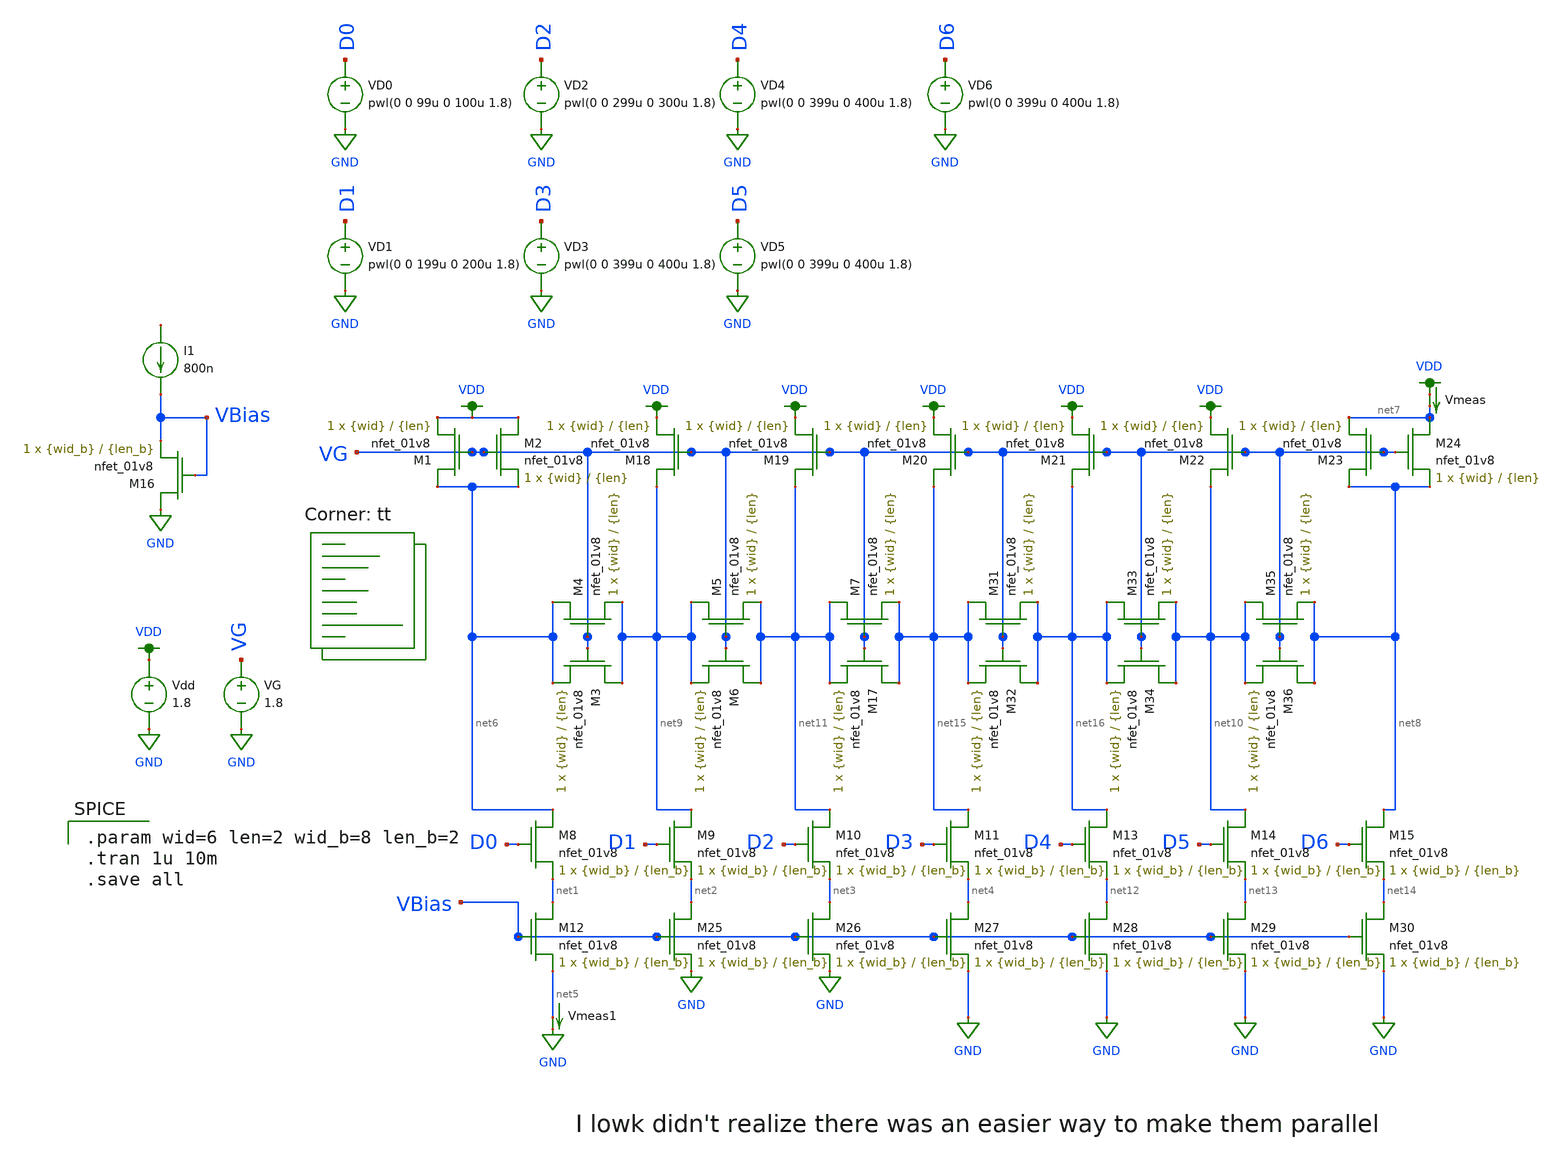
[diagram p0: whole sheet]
** sch_path: mp3/ladder_tb.sch
**.subckt ladder_tb
XM8 net6 D0 net1 GND sky130_fd_pr__nfet_01v8 L={len_b} W={wid_b} nf=1 ad='int((nf+1)/2) * W/nf * 0.29'
+ as='int((nf+2)/2) * W/nf * 0.29' pd='2*int((nf+1)/2) * (W/nf + 0.29)' ps='2*int((nf+2)/2) * (W/nf + 0.29)'
+ nrd='0.29 / W' nrs='0.29 / W' sa=0 sb=0 sd=0 mult=1 m=1
Vmeas1 net5 GND 0
.save i(vmeas1)
Vdd VDD GND 1.8
VG VG GND 1.8
VD0 D0 GND pwl(0 0 99u 0 100u 1.8)
VD1 D1 GND pwl(0 0 199u 0 200u 1.8)
VD2 D2 GND pwl(0 0 299u 0 300u 1.8)
VD3 D3 GND pwl(0 0 399u 0 400u 1.8)
XM16 GND VBias VBias GND sky130_fd_pr__nfet_01v8 L={len_b} W={wid_b} nf=1 ad='int((nf+1)/2) * W/nf * 0.29'
+ as='int((nf+2)/2) * W/nf * 0.29' pd='2*int((nf+1)/2) * (W/nf + 0.29)' ps='2*int((nf+2)/2) * (W/nf + 0.29)'
+ nrd='0.29 / W' nrs='0.29 / W' sa=0 sb=0 sd=0 mult=1 m=1
I1 net17 VBias 800n
XM1 net6 VG VDD GND sky130_fd_pr__nfet_01v8 L={len} W={wid} nf=1 ad='int((nf+1)/2) * W/nf * 0.29' as='int((nf+2)/2) * W/nf * 0.29'
+ pd='2*int((nf+1)/2) * (W/nf + 0.29)' ps='2*int((nf+2)/2) * (W/nf + 0.29)' nrd='0.29 / W' nrs='0.29 / W'
+ sa=0 sb=0 sd=0 mult=1 m=1
XM4 net6 VG net9 GND sky130_fd_pr__nfet_01v8 L={len} W={wid} nf=1 ad='int((nf+1)/2) * W/nf * 0.29' as='int((nf+2)/2) * W/nf * 0.29'
+ pd='2*int((nf+1)/2) * (W/nf + 0.29)' ps='2*int((nf+2)/2) * (W/nf + 0.29)' nrd='0.29 / W' nrs='0.29 / W'
+ sa=0 sb=0 sd=0 mult=1 m=1
Vmeas VDD net7 0
.save i(vmeas)
VD4 D4 GND pwl(0 0 399u 0 400u 1.8)
VD5 D5 GND pwl(0 0 399u 0 400u 1.8)
VD6 D6 GND pwl(0 0 399u 0 400u 1.8)
XM12 net1 VBias net5 GND sky130_fd_pr__nfet_01v8 L={len_b} W={wid_b} nf=1 ad='int((nf+1)/2) * W/nf * 0.29'
+ as='int((nf+2)/2) * W/nf * 0.29' pd='2*int((nf+1)/2) * (W/nf + 0.29)' ps='2*int((nf+2)/2) * (W/nf + 0.29)'
+ nrd='0.29 / W' nrs='0.29 / W' sa=0 sb=0 sd=0 mult=1 m=1
XM9 net9 D1 net2 GND sky130_fd_pr__nfet_01v8 L={len_b} W={wid_b} nf=1 ad='int((nf+1)/2) * W/nf * 0.29'
+ as='int((nf+2)/2) * W/nf * 0.29' pd='2*int((nf+1)/2) * (W/nf + 0.29)' ps='2*int((nf+2)/2) * (W/nf + 0.29)'
+ nrd='0.29 / W' nrs='0.29 / W' sa=0 sb=0 sd=0 mult=1 m=1
XM10 net11 D2 net3 GND sky130_fd_pr__nfet_01v8 L={len_b} W={wid_b} nf=1 ad='int((nf+1)/2) * W/nf * 0.29'
+ as='int((nf+2)/2) * W/nf * 0.29' pd='2*int((nf+1)/2) * (W/nf + 0.29)' ps='2*int((nf+2)/2) * (W/nf + 0.29)'
+ nrd='0.29 / W' nrs='0.29 / W' sa=0 sb=0 sd=0 mult=1 m=1
XM11 net15 D3 net4 GND sky130_fd_pr__nfet_01v8 L={len_b} W={wid_b} nf=1 ad='int((nf+1)/2) * W/nf * 0.29'
+ as='int((nf+2)/2) * W/nf * 0.29' pd='2*int((nf+1)/2) * (W/nf + 0.29)' ps='2*int((nf+2)/2) * (W/nf + 0.29)'
+ nrd='0.29 / W' nrs='0.29 / W' sa=0 sb=0 sd=0 mult=1 m=1
XM13 net16 D4 net12 GND sky130_fd_pr__nfet_01v8 L={len_b} W={wid_b} nf=1 ad='int((nf+1)/2) * W/nf * 0.29'
+ as='int((nf+2)/2) * W/nf * 0.29' pd='2*int((nf+1)/2) * (W/nf + 0.29)' ps='2*int((nf+2)/2) * (W/nf + 0.29)'
+ nrd='0.29 / W' nrs='0.29 / W' sa=0 sb=0 sd=0 mult=1 m=1
XM14 net10 D5 net13 GND sky130_fd_pr__nfet_01v8 L={len_b} W={wid_b} nf=1 ad='int((nf+1)/2) * W/nf * 0.29'
+ as='int((nf+2)/2) * W/nf * 0.29' pd='2*int((nf+1)/2) * (W/nf + 0.29)' ps='2*int((nf+2)/2) * (W/nf + 0.29)'
+ nrd='0.29 / W' nrs='0.29 / W' sa=0 sb=0 sd=0 mult=1 m=1
XM15 net8 D6 net14 GND sky130_fd_pr__nfet_01v8 L={len_b} W={wid_b} nf=1 ad='int((nf+1)/2) * W/nf * 0.29'
+ as='int((nf+2)/2) * W/nf * 0.29' pd='2*int((nf+1)/2) * (W/nf + 0.29)' ps='2*int((nf+2)/2) * (W/nf + 0.29)'
+ nrd='0.29 / W' nrs='0.29 / W' sa=0 sb=0 sd=0 mult=1 m=1
XM25 net2 VBias GND GND sky130_fd_pr__nfet_01v8 L={len_b} W={wid_b} nf=1 ad='int((nf+1)/2) * W/nf * 0.29'
+ as='int((nf+2)/2) * W/nf * 0.29' pd='2*int((nf+1)/2) * (W/nf + 0.29)' ps='2*int((nf+2)/2) * (W/nf + 0.29)'
+ nrd='0.29 / W' nrs='0.29 / W' sa=0 sb=0 sd=0 mult=1 m=1
XM26 net3 VBias GND GND sky130_fd_pr__nfet_01v8 L={len_b} W={wid_b} nf=1 ad='int((nf+1)/2) * W/nf * 0.29'
+ as='int((nf+2)/2) * W/nf * 0.29' pd='2*int((nf+1)/2) * (W/nf + 0.29)' ps='2*int((nf+2)/2) * (W/nf + 0.29)'
+ nrd='0.29 / W' nrs='0.29 / W' sa=0 sb=0 sd=0 mult=1 m=1
XM27 net4 VBias GND GND sky130_fd_pr__nfet_01v8 L={len_b} W={wid_b} nf=1 ad='int((nf+1)/2) * W/nf * 0.29'
+ as='int((nf+2)/2) * W/nf * 0.29' pd='2*int((nf+1)/2) * (W/nf + 0.29)' ps='2*int((nf+2)/2) * (W/nf + 0.29)'
+ nrd='0.29 / W' nrs='0.29 / W' sa=0 sb=0 sd=0 mult=1 m=1
XM28 net12 VBias GND GND sky130_fd_pr__nfet_01v8 L={len_b} W={wid_b} nf=1 ad='int((nf+1)/2) * W/nf * 0.29'
+ as='int((nf+2)/2) * W/nf * 0.29' pd='2*int((nf+1)/2) * (W/nf + 0.29)' ps='2*int((nf+2)/2) * (W/nf + 0.29)'
+ nrd='0.29 / W' nrs='0.29 / W' sa=0 sb=0 sd=0 mult=1 m=1
XM29 net13 VBias GND GND sky130_fd_pr__nfet_01v8 L={len_b} W={wid_b} nf=1 ad='int((nf+1)/2) * W/nf * 0.29'
+ as='int((nf+2)/2) * W/nf * 0.29' pd='2*int((nf+1)/2) * (W/nf + 0.29)' ps='2*int((nf+2)/2) * (W/nf + 0.29)'
+ nrd='0.29 / W' nrs='0.29 / W' sa=0 sb=0 sd=0 mult=1 m=1
XM30 net14 VBias GND GND sky130_fd_pr__nfet_01v8 L={len_b} W={wid_b} nf=1 ad='int((nf+1)/2) * W/nf * 0.29'
+ as='int((nf+2)/2) * W/nf * 0.29' pd='2*int((nf+1)/2) * (W/nf + 0.29)' ps='2*int((nf+2)/2) * (W/nf + 0.29)'
+ nrd='0.29 / W' nrs='0.29 / W' sa=0 sb=0 sd=0 mult=1 m=1
XM2 VDD VG net6 GND sky130_fd_pr__nfet_01v8 L={len} W={wid} nf=1 ad='int((nf+1)/2) * W/nf * 0.29' as='int((nf+2)/2) * W/nf * 0.29'
+ pd='2*int((nf+1)/2) * (W/nf + 0.29)' ps='2*int((nf+2)/2) * (W/nf + 0.29)' nrd='0.29 / W' nrs='0.29 / W'
+ sa=0 sb=0 sd=0 mult=1 m=1
XM18 net9 VG VDD GND sky130_fd_pr__nfet_01v8 L={len} W={wid} nf=1 ad='int((nf+1)/2) * W/nf * 0.29' as='int((nf+2)/2) * W/nf * 0.29'
+ pd='2*int((nf+1)/2) * (W/nf + 0.29)' ps='2*int((nf+2)/2) * (W/nf + 0.29)' nrd='0.29 / W' nrs='0.29 / W'
+ sa=0 sb=0 sd=0 mult=1 m=1
XM19 net11 VG VDD GND sky130_fd_pr__nfet_01v8 L={len} W={wid} nf=1 ad='int((nf+1)/2) * W/nf * 0.29' as='int((nf+2)/2) * W/nf * 0.29'
+ pd='2*int((nf+1)/2) * (W/nf + 0.29)' ps='2*int((nf+2)/2) * (W/nf + 0.29)' nrd='0.29 / W' nrs='0.29 / W'
+ sa=0 sb=0 sd=0 mult=1 m=1
XM20 net15 VG VDD GND sky130_fd_pr__nfet_01v8 L={len} W={wid} nf=1 ad='int((nf+1)/2) * W/nf * 0.29' as='int((nf+2)/2) * W/nf * 0.29'
+ pd='2*int((nf+1)/2) * (W/nf + 0.29)' ps='2*int((nf+2)/2) * (W/nf + 0.29)' nrd='0.29 / W' nrs='0.29 / W'
+ sa=0 sb=0 sd=0 mult=1 m=1
XM21 net16 VG VDD GND sky130_fd_pr__nfet_01v8 L={len} W={wid} nf=1 ad='int((nf+1)/2) * W/nf * 0.29' as='int((nf+2)/2) * W/nf * 0.29'
+ pd='2*int((nf+1)/2) * (W/nf + 0.29)' ps='2*int((nf+2)/2) * (W/nf + 0.29)' nrd='0.29 / W' nrs='0.29 / W'
+ sa=0 sb=0 sd=0 mult=1 m=1
XM22 net10 VG VDD GND sky130_fd_pr__nfet_01v8 L={len} W={wid} nf=1 ad='int((nf+1)/2) * W/nf * 0.29' as='int((nf+2)/2) * W/nf * 0.29'
+ pd='2*int((nf+1)/2) * (W/nf + 0.29)' ps='2*int((nf+2)/2) * (W/nf + 0.29)' nrd='0.29 / W' nrs='0.29 / W'
+ sa=0 sb=0 sd=0 mult=1 m=1
XM23 net8 VG net7 GND sky130_fd_pr__nfet_01v8 L={len} W={wid} nf=1 ad='int((nf+1)/2) * W/nf * 0.29' as='int((nf+2)/2) * W/nf * 0.29'
+ pd='2*int((nf+1)/2) * (W/nf + 0.29)' ps='2*int((nf+2)/2) * (W/nf + 0.29)' nrd='0.29 / W' nrs='0.29 / W'
+ sa=0 sb=0 sd=0 mult=1 m=1
XM24 net7 VG net8 GND sky130_fd_pr__nfet_01v8 L={len} W={wid} nf=1 ad='int((nf+1)/2) * W/nf * 0.29' as='int((nf+2)/2) * W/nf * 0.29'
+ pd='2*int((nf+1)/2) * (W/nf + 0.29)' ps='2*int((nf+2)/2) * (W/nf + 0.29)' nrd='0.29 / W' nrs='0.29 / W'
+ sa=0 sb=0 sd=0 mult=1 m=1
XM3 net9 VG net6 GND sky130_fd_pr__nfet_01v8 L={len} W={wid} nf=1 ad='int((nf+1)/2) * W/nf * 0.29' as='int((nf+2)/2) * W/nf * 0.29'
+ pd='2*int((nf+1)/2) * (W/nf + 0.29)' ps='2*int((nf+2)/2) * (W/nf + 0.29)' nrd='0.29 / W' nrs='0.29 / W'
+ sa=0 sb=0 sd=0 mult=1 m=1
XM5 net9 VG net11 GND sky130_fd_pr__nfet_01v8 L={len} W={wid} nf=1 ad='int((nf+1)/2) * W/nf * 0.29' as='int((nf+2)/2) * W/nf * 0.29'
+ pd='2*int((nf+1)/2) * (W/nf + 0.29)' ps='2*int((nf+2)/2) * (W/nf + 0.29)' nrd='0.29 / W' nrs='0.29 / W'
+ sa=0 sb=0 sd=0 mult=1 m=1
XM6 net11 VG net9 GND sky130_fd_pr__nfet_01v8 L={len} W={wid} nf=1 ad='int((nf+1)/2) * W/nf * 0.29' as='int((nf+2)/2) * W/nf * 0.29'
+ pd='2*int((nf+1)/2) * (W/nf + 0.29)' ps='2*int((nf+2)/2) * (W/nf + 0.29)' nrd='0.29 / W' nrs='0.29 / W'
+ sa=0 sb=0 sd=0 mult=1 m=1
XM7 net11 VG net15 GND sky130_fd_pr__nfet_01v8 L={len} W={wid} nf=1 ad='int((nf+1)/2) * W/nf * 0.29'
+ as='int((nf+2)/2) * W/nf * 0.29' pd='2*int((nf+1)/2) * (W/nf + 0.29)' ps='2*int((nf+2)/2) * (W/nf + 0.29)'
+ nrd='0.29 / W' nrs='0.29 / W' sa=0 sb=0 sd=0 mult=1 m=1
XM17 net15 VG net11 GND sky130_fd_pr__nfet_01v8 L={len} W={wid} nf=1 ad='int((nf+1)/2) * W/nf * 0.29'
+ as='int((nf+2)/2) * W/nf * 0.29' pd='2*int((nf+1)/2) * (W/nf + 0.29)' ps='2*int((nf+2)/2) * (W/nf + 0.29)'
+ nrd='0.29 / W' nrs='0.29 / W' sa=0 sb=0 sd=0 mult=1 m=1
XM31 net15 VG net16 GND sky130_fd_pr__nfet_01v8 L={len} W={wid} nf=1 ad='int((nf+1)/2) * W/nf * 0.29'
+ as='int((nf+2)/2) * W/nf * 0.29' pd='2*int((nf+1)/2) * (W/nf + 0.29)' ps='2*int((nf+2)/2) * (W/nf + 0.29)'
+ nrd='0.29 / W' nrs='0.29 / W' sa=0 sb=0 sd=0 mult=1 m=1
XM32 net16 VG net15 GND sky130_fd_pr__nfet_01v8 L={len} W={wid} nf=1 ad='int((nf+1)/2) * W/nf * 0.29'
+ as='int((nf+2)/2) * W/nf * 0.29' pd='2*int((nf+1)/2) * (W/nf + 0.29)' ps='2*int((nf+2)/2) * (W/nf + 0.29)'
+ nrd='0.29 / W' nrs='0.29 / W' sa=0 sb=0 sd=0 mult=1 m=1
XM33 net16 VG net10 GND sky130_fd_pr__nfet_01v8 L={len} W={wid} nf=1 ad='int((nf+1)/2) * W/nf * 0.29'
+ as='int((nf+2)/2) * W/nf * 0.29' pd='2*int((nf+1)/2) * (W/nf + 0.29)' ps='2*int((nf+2)/2) * (W/nf + 0.29)'
+ nrd='0.29 / W' nrs='0.29 / W' sa=0 sb=0 sd=0 mult=1 m=1
XM34 net10 VG net16 GND sky130_fd_pr__nfet_01v8 L={len} W={wid} nf=1 ad='int((nf+1)/2) * W/nf * 0.29'
+ as='int((nf+2)/2) * W/nf * 0.29' pd='2*int((nf+1)/2) * (W/nf + 0.29)' ps='2*int((nf+2)/2) * (W/nf + 0.29)'
+ nrd='0.29 / W' nrs='0.29 / W' sa=0 sb=0 sd=0 mult=1 m=1
XM35 net10 VG net8 GND sky130_fd_pr__nfet_01v8 L={len} W={wid} nf=1 ad='int((nf+1)/2) * W/nf * 0.29'
+ as='int((nf+2)/2) * W/nf * 0.29' pd='2*int((nf+1)/2) * (W/nf + 0.29)' ps='2*int((nf+2)/2) * (W/nf + 0.29)'
+ nrd='0.29 / W' nrs='0.29 / W' sa=0 sb=0 sd=0 mult=1 m=1
XM36 net8 VG net10 GND sky130_fd_pr__nfet_01v8 L={len} W={wid} nf=1 ad='int((nf+1)/2) * W/nf * 0.29'
+ as='int((nf+2)/2) * W/nf * 0.29' pd='2*int((nf+1)/2) * (W/nf + 0.29)' ps='2*int((nf+2)/2) * (W/nf + 0.29)'
+ nrd='0.29 / W' nrs='0.29 / W' sa=0 sb=0 sd=0 mult=1 m=1
**** begin user architecture code

.param wid=6 len=2 wid_b=8 len_b=2
.tran 1u 10m
.save all


.lib $::SKYWATER_MODELS/sky130.lib.spice tt
**** end user architecture code
**.ends
.GLOBAL GND
.GLOBAL VDD
.end
